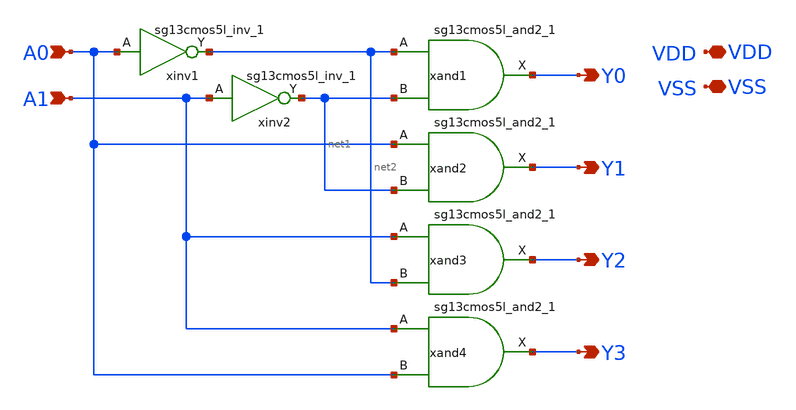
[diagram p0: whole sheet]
** sch_path: archives/dec2to4/dec2to4.sch
**.subckt dec2to4 A0 A1 Y0 Y1 Y2 Y3 VDD VSS
*.ipin A0
*.ipin A1
*.opin Y0
*.opin Y1
*.opin Y2
*.opin Y3
*.iopin VDD
*.iopin VSS
xinv1 net2 A0 VDD VSS sg13cmos5l_inv_1
xinv2 net1 A1 VDD VSS sg13cmos5l_inv_1
xand1 Y0 net2 net1 VDD VSS sg13cmos5l_and2_1
xand2 Y1 A0 net1 VDD VSS sg13cmos5l_and2_1
xand3 Y2 A1 net2 VDD VSS sg13cmos5l_and2_1
xand4 Y3 A1 A0 VDD VSS sg13cmos5l_and2_1
**.ends
.end
